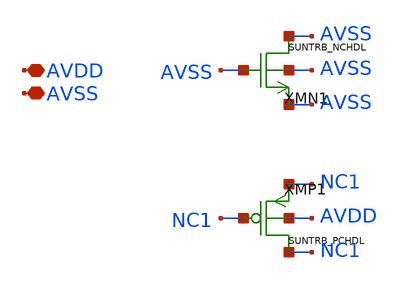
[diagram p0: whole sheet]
** sch_path: design/SUN_TRB_SKY130NM/SUNTRB_TAPCELLBAVSS_CV.sch
**.subckt SUNTRB_TAPCELLBAVSS_CV AVDD AVSS
*.iopin AVDD
*.iopin AVSS
XMN1 AVSS AVSS AVSS AVSS SUNTRB_NCHDL xoffset=0 yoffset=0 angle=0
XMP1 NC1 NC1 NC1 AVDD SUNTRB_PCHDL xoffset=0 yoffset=0 angle=0 M=1
**.ends
.end
